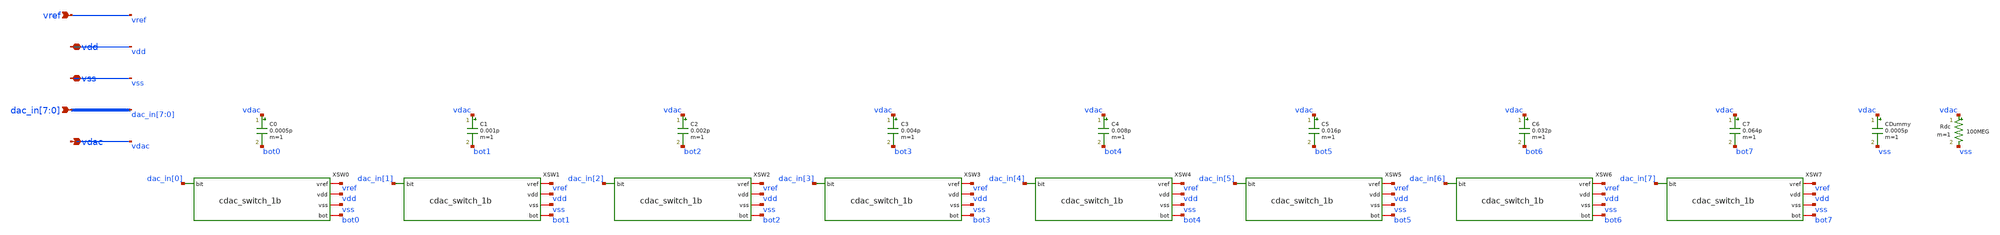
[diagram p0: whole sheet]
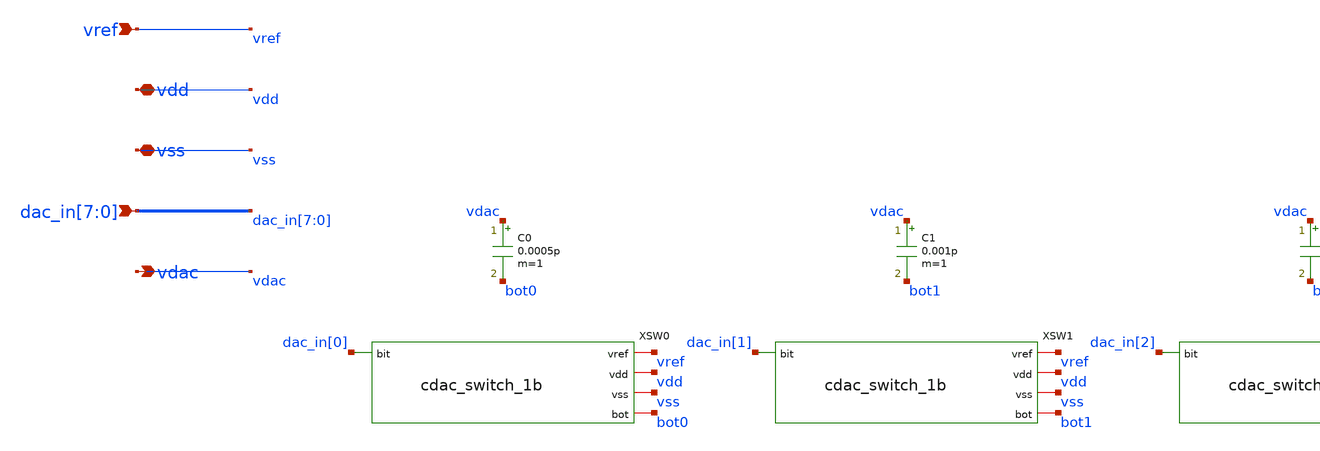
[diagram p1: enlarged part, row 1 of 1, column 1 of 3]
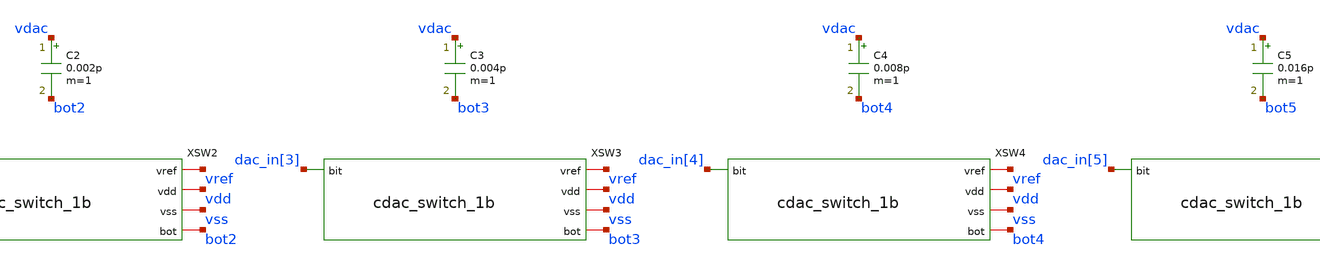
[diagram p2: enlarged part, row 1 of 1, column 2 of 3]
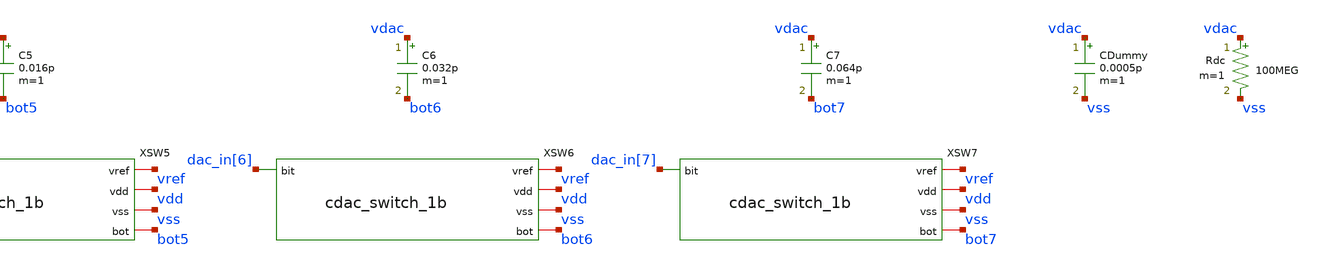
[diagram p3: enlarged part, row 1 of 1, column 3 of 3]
** sch_path: xschem/sar_adc/blocks/cdac/cdac_8bit.sch
**.subckt cdac_8bit vref vdd vss
*+ dac_in[7],dac_in[6],dac_in[5],dac_in[4],dac_in[3],dac_in[2],dac_in[1],dac_in[0] vdac
*.ipin vref
*.iopin vdd
*.iopin vss
*.ipin dac_in[7],dac_in[6],dac_in[5],dac_in[4],dac_in[3],dac_in[2],dac_in[1],dac_in[0]
*.opin vdac
XSW0 dac_in[0] vref vdd vss bot0 cdac_switch_1b
C0 vdac bot0 0.0005p m=1
XSW1 dac_in[1] vref vdd vss bot1 cdac_switch_1b
C1 vdac bot1 0.001p m=1
XSW2 dac_in[2] vref vdd vss bot2 cdac_switch_1b
C2 vdac bot2 0.002p m=1
XSW3 dac_in[3] vref vdd vss bot3 cdac_switch_1b
C3 vdac bot3 0.004p m=1
XSW4 dac_in[4] vref vdd vss bot4 cdac_switch_1b
C4 vdac bot4 0.008p m=1
XSW5 dac_in[5] vref vdd vss bot5 cdac_switch_1b
C5 vdac bot5 0.016p m=1
XSW6 dac_in[6] vref vdd vss bot6 cdac_switch_1b
C6 vdac bot6 0.032p m=1
XSW7 dac_in[7] vref vdd vss bot7 cdac_switch_1b
C7 vdac bot7 0.064p m=1
CDummy vdac vss 0.0005p m=1
Rdc vdac vss 100MEG m=1
**.ends

* expanding   symbol:  sar_adc/blocks/cdac/cdac_switch_1b.sym # of pins=5
** sym_path: xschem/sar_adc/blocks/cdac/cdac_switch_1b.sym
** sch_path: xschem/sar_adc/blocks/cdac/cdac_switch_1b.sch
.subckt cdac_switch_1b bit vref vdd vss bot
*.ipin bit
*.iopin vref
*.iopin vdd
*.iopin vss
*.iopin bot
XM1 bit_b bit vdd vdd pfet_03v3 L=0.28u W=0.8u nf=1 ad='int((nf+1)/2) * W/nf * 0.18u' as='int((nf+2)/2) * W/nf * 0.18u'
+ pd='2*int((nf+1)/2) * (W/nf + 0.18u)' ps='2*int((nf+2)/2) * (W/nf + 0.18u)' nrd='0.18u / W' nrs='0.18u / W'
+ sa=0 sb=0 sd=0 m=1
XM2 bit_b bit vss vss nfet_03v3 L=0.28u W=0.4u nf=1 ad='int((nf+1)/2) * W/nf * 0.18u' as='int((nf+2)/2) * W/nf * 0.18u'
+ pd='2*int((nf+1)/2) * (W/nf + 0.18u)' ps='2*int((nf+2)/2) * (W/nf + 0.18u)' nrd='0.18u / W' nrs='0.18u / W'
+ sa=0 sb=0 sd=0 m=1
XM3 bot bit_b vref vdd pfet_03v3 L=0.28u W=2.0u nf=1 ad='int((nf+1)/2) * W/nf * 0.18u' as='int((nf+2)/2) * W/nf * 0.18u'
+ pd='2*int((nf+1)/2) * (W/nf + 0.18u)' ps='2*int((nf+2)/2) * (W/nf + 0.18u)' nrd='0.18u / W' nrs='0.18u / W'
+ sa=0 sb=0 sd=0 m=1
XM4 vref bit bot vss nfet_03v3 L=0.28u W=1.0u nf=1 ad='int((nf+1)/2) * W/nf * 0.18u' as='int((nf+2)/2) * W/nf * 0.18u'
+ pd='2*int((nf+1)/2) * (W/nf + 0.18u)' ps='2*int((nf+2)/2) * (W/nf + 0.18u)' nrd='0.18u / W' nrs='0.18u / W'
+ sa=0 sb=0 sd=0 m=1
XM5 bot bit vss vdd pfet_03v3 L=0.28u W=2.0u nf=1 ad='int((nf+1)/2) * W/nf * 0.18u' as='int((nf+2)/2) * W/nf * 0.18u'
+ pd='2*int((nf+1)/2) * (W/nf + 0.18u)' ps='2*int((nf+2)/2) * (W/nf + 0.18u)' nrd='0.18u / W' nrs='0.18u / W'
+ sa=0 sb=0 sd=0 m=1
XM6 vss bit_b bot vss nfet_03v3 L=0.28u W=1.0u nf=1 ad='int((nf+1)/2) * W/nf * 0.18u' as='int((nf+2)/2) * W/nf * 0.18u'
+ pd='2*int((nf+1)/2) * (W/nf + 0.18u)' ps='2*int((nf+2)/2) * (W/nf + 0.18u)' nrd='0.18u / W' nrs='0.18u / W'
+ sa=0 sb=0 sd=0 m=1
.ends

.end
